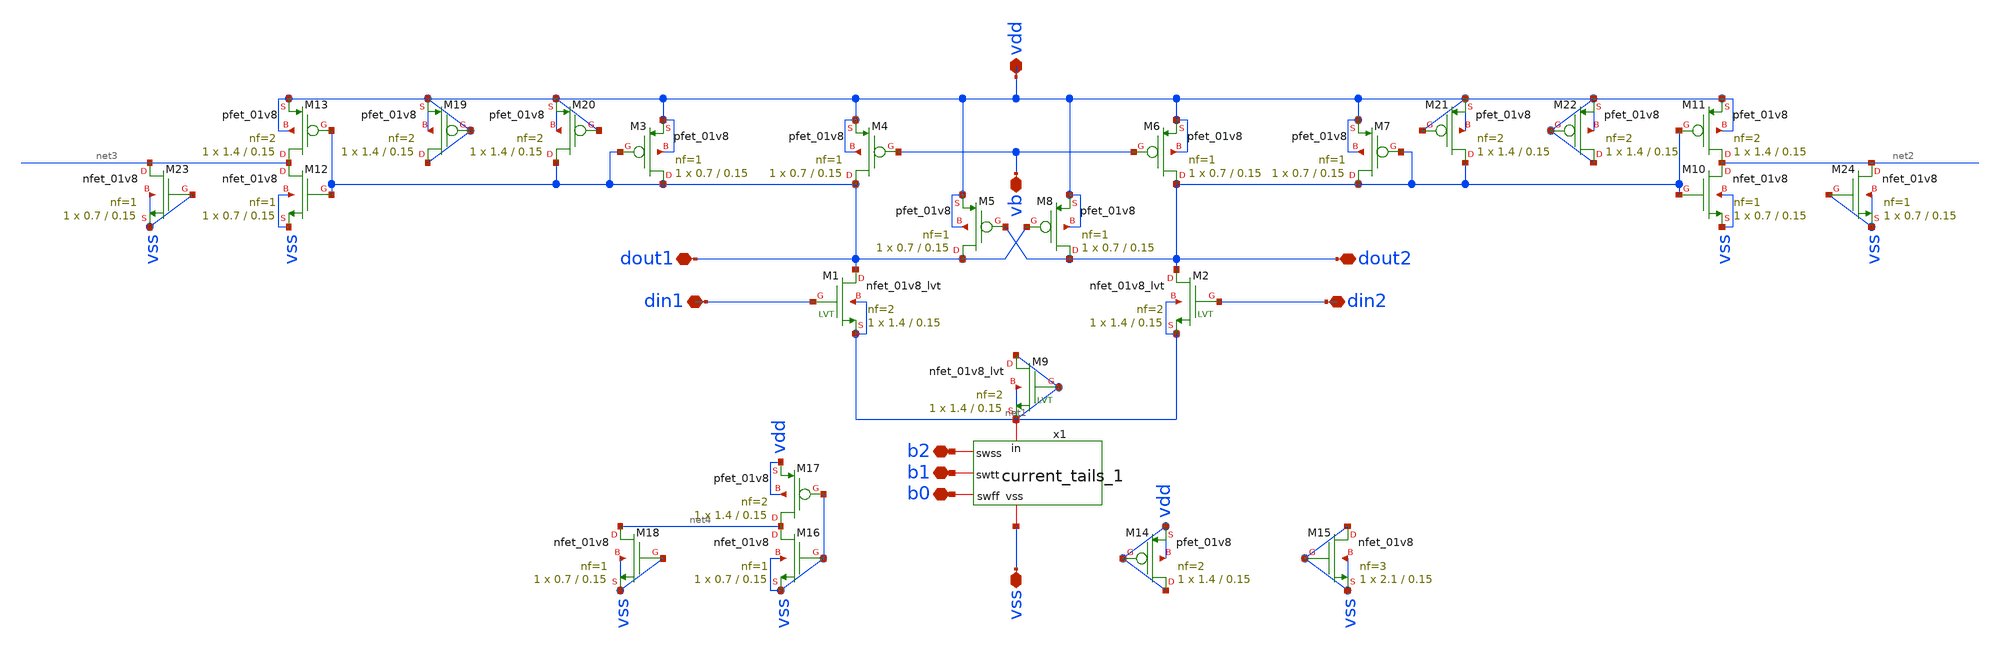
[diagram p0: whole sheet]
** sch_path: xschem/delay_cell_4.sch
**.subckt delay_cell_4 vdd vss vb din1 din2 dout2 dout1 b2 b1 b0
*.iopin vdd
*.iopin vss
*.iopin vb
*.iopin din1
*.iopin din2
*.iopin dout2
*.iopin dout1
*.iopin b2
*.iopin b1
*.iopin b0
XM5 dout1 dout2 vdd vdd sky130_fd_pr__pfet_01v8 L=0.15 W=0.7 nf=1 ad='int((nf+1)/2) * W/nf * 0.29' as='int((nf+2)/2) * W/nf * 0.29'
+ pd='2*int((nf+1)/2) * (W/nf + 0.29)' ps='2*int((nf+2)/2) * (W/nf + 0.29)' nrd='0.29 / W' nrs='0.29 / W'
+ sa=0 sb=0 sd=0 mult=1 m=1
XM8 dout2 dout1 vdd vdd sky130_fd_pr__pfet_01v8 L=0.15 W=0.7 nf=1 ad='int((nf+1)/2) * W/nf * 0.29' as='int((nf+2)/2) * W/nf * 0.29'
+ pd='2*int((nf+1)/2) * (W/nf + 0.29)' ps='2*int((nf+2)/2) * (W/nf + 0.29)' nrd='0.29 / W' nrs='0.29 / W'
+ sa=0 sb=0 sd=0 mult=1 m=1
XM3 dout1 dout1 vdd vdd sky130_fd_pr__pfet_01v8 L=0.15 W=0.7 nf=1 ad='int((nf+1)/2) * W/nf * 0.29' as='int((nf+2)/2) * W/nf * 0.29'
+ pd='2*int((nf+1)/2) * (W/nf + 0.29)' ps='2*int((nf+2)/2) * (W/nf + 0.29)' nrd='0.29 / W' nrs='0.29 / W'
+ sa=0 sb=0 sd=0 mult=1 m=1
XM4 dout1 vb vdd vdd sky130_fd_pr__pfet_01v8 L=0.15 W=0.7 nf=1 ad='int((nf+1)/2) * W/nf * 0.29' as='int((nf+2)/2) * W/nf * 0.29'
+ pd='2*int((nf+1)/2) * (W/nf + 0.29)' ps='2*int((nf+2)/2) * (W/nf + 0.29)' nrd='0.29 / W' nrs='0.29 / W'
+ sa=0 sb=0 sd=0 mult=1 m=1
XM6 dout2 vb vdd vdd sky130_fd_pr__pfet_01v8 L=0.15 W=0.7 nf=1 ad='int((nf+1)/2) * W/nf * 0.29' as='int((nf+2)/2) * W/nf * 0.29'
+ pd='2*int((nf+1)/2) * (W/nf + 0.29)' ps='2*int((nf+2)/2) * (W/nf + 0.29)' nrd='0.29 / W' nrs='0.29 / W'
+ sa=0 sb=0 sd=0 mult=1 m=1
XM7 dout2 dout2 vdd vdd sky130_fd_pr__pfet_01v8 L=0.15 W=0.7 nf=1 ad='int((nf+1)/2) * W/nf * 0.29' as='int((nf+2)/2) * W/nf * 0.29'
+ pd='2*int((nf+1)/2) * (W/nf + 0.29)' ps='2*int((nf+2)/2) * (W/nf + 0.29)' nrd='0.29 / W' nrs='0.29 / W'
+ sa=0 sb=0 sd=0 mult=1 m=1
XM1 dout1 din1 net1 net1 sky130_fd_pr__nfet_01v8_lvt L=0.15 W=1.4 nf=2 ad='int((nf+1)/2) * W/nf * 0.29'
+ as='int((nf+2)/2) * W/nf * 0.29' pd='2*int((nf+1)/2) * (W/nf + 0.29)' ps='2*int((nf+2)/2) * (W/nf + 0.29)'
+ nrd='0.29 / W' nrs='0.29 / W' sa=0 sb=0 sd=0 mult=1 m=1
XM2 dout2 din2 net1 net1 sky130_fd_pr__nfet_01v8_lvt L=0.15 W=1.4 nf=2 ad='int((nf+1)/2) * W/nf * 0.29'
+ as='int((nf+2)/2) * W/nf * 0.29' pd='2*int((nf+1)/2) * (W/nf + 0.29)' ps='2*int((nf+2)/2) * (W/nf + 0.29)'
+ nrd='0.29 / W' nrs='0.29 / W' sa=0 sb=0 sd=0 mult=1 m=1
XM9 net1 net1 net1 net1 sky130_fd_pr__nfet_01v8_lvt L=0.15 W=1.4 nf=2 ad='int((nf+1)/2) * W/nf * 0.29'
+ as='int((nf+2)/2) * W/nf * 0.29' pd='2*int((nf+1)/2) * (W/nf + 0.29)' ps='2*int((nf+2)/2) * (W/nf + 0.29)'
+ nrd='0.29 / W' nrs='0.29 / W' sa=0 sb=0 sd=0 mult=1 m=1
x1 net1 b2 vss b1 b0 current_tails_1
XM10 net2 dout2 vss vss sky130_fd_pr__nfet_01v8 L=0.15 W=0.7 nf=1 ad='int((nf+1)/2) * W/nf * 0.29' as='int((nf+2)/2) * W/nf * 0.29'
+ pd='2*int((nf+1)/2) * (W/nf + 0.29)' ps='2*int((nf+2)/2) * (W/nf + 0.29)' nrd='0.29 / W' nrs='0.29 / W'
+ sa=0 sb=0 sd=0 mult=1 m=1
XM11 net2 dout2 vdd vdd sky130_fd_pr__pfet_01v8 L=0.15 W=1.4 nf=2 ad='int((nf+1)/2) * W/nf * 0.29' as='int((nf+2)/2) * W/nf * 0.29'
+ pd='2*int((nf+1)/2) * (W/nf + 0.29)' ps='2*int((nf+2)/2) * (W/nf + 0.29)' nrd='0.29 / W' nrs='0.29 / W'
+ sa=0 sb=0 sd=0 mult=1 m=1
XM12 net3 dout1 vss vss sky130_fd_pr__nfet_01v8 L=0.15 W=0.7 nf=1 ad='int((nf+1)/2) * W/nf * 0.29' as='int((nf+2)/2) * W/nf * 0.29'
+ pd='2*int((nf+1)/2) * (W/nf + 0.29)' ps='2*int((nf+2)/2) * (W/nf + 0.29)' nrd='0.29 / W' nrs='0.29 / W'
+ sa=0 sb=0 sd=0 mult=1 m=1
XM13 net3 dout1 vdd vdd sky130_fd_pr__pfet_01v8 L=0.15 W=1.4 nf=2 ad='int((nf+1)/2) * W/nf * 0.29' as='int((nf+2)/2) * W/nf * 0.29'
+ pd='2*int((nf+1)/2) * (W/nf + 0.29)' ps='2*int((nf+2)/2) * (W/nf + 0.29)' nrd='0.29 / W' nrs='0.29 / W'
+ sa=0 sb=0 sd=0 mult=1 m=1
XM14 vdd vdd vdd vdd sky130_fd_pr__pfet_01v8 L=0.15 W=1.4 nf=2 ad='int((nf+1)/2) * W/nf * 0.29' as='int((nf+2)/2) * W/nf * 0.29'
+ pd='2*int((nf+1)/2) * (W/nf + 0.29)' ps='2*int((nf+2)/2) * (W/nf + 0.29)' nrd='0.29 / W' nrs='0.29 / W'
+ sa=0 sb=0 sd=0 mult=1 m=1
XM15 vss vss vss vss sky130_fd_pr__nfet_01v8 L=0.15 W=2.1 nf=3 ad='int((nf+1)/2) * W/nf * 0.29' as='int((nf+2)/2) * W/nf * 0.29'
+ pd='2*int((nf+1)/2) * (W/nf + 0.29)' ps='2*int((nf+2)/2) * (W/nf + 0.29)' nrd='0.29 / W' nrs='0.29 / W'
+ sa=0 sb=0 sd=0 mult=1 m=1
XM16 net4 vss vss vss sky130_fd_pr__nfet_01v8 L=0.15 W=0.7 nf=1 ad='int((nf+1)/2) * W/nf * 0.29' as='int((nf+2)/2) * W/nf * 0.29'
+ pd='2*int((nf+1)/2) * (W/nf + 0.29)' ps='2*int((nf+2)/2) * (W/nf + 0.29)' nrd='0.29 / W' nrs='0.29 / W'
+ sa=0 sb=0 sd=0 mult=1 m=1
XM17 net4 vss vdd vdd sky130_fd_pr__pfet_01v8 L=0.15 W=1.4 nf=2 ad='int((nf+1)/2) * W/nf * 0.29' as='int((nf+2)/2) * W/nf * 0.29'
+ pd='2*int((nf+1)/2) * (W/nf + 0.29)' ps='2*int((nf+2)/2) * (W/nf + 0.29)' nrd='0.29 / W' nrs='0.29 / W'
+ sa=0 sb=0 sd=0 mult=1 m=1
XM21 dout2 vdd vdd vdd sky130_fd_pr__pfet_01v8 L=0.15 W=1.4 nf=2 ad='int((nf+1)/2) * W/nf * 0.29' as='int((nf+2)/2) * W/nf * 0.29'
+ pd='2*int((nf+1)/2) * (W/nf + 0.29)' ps='2*int((nf+2)/2) * (W/nf + 0.29)' nrd='0.29 / W' nrs='0.29 / W'
+ sa=0 sb=0 sd=0 mult=1 m=1
XM20 dout1 vdd vdd vdd sky130_fd_pr__pfet_01v8 L=0.15 W=1.4 nf=2 ad='int((nf+1)/2) * W/nf * 0.29' as='int((nf+2)/2) * W/nf * 0.29'
+ pd='2*int((nf+1)/2) * (W/nf + 0.29)' ps='2*int((nf+2)/2) * (W/nf + 0.29)' nrd='0.29 / W' nrs='0.29 / W'
+ sa=0 sb=0 sd=0 mult=1 m=1
XM22 vdd vdd vdd vdd sky130_fd_pr__pfet_01v8 L=0.15 W=1.4 nf=2 ad='int((nf+1)/2) * W/nf * 0.29' as='int((nf+2)/2) * W/nf * 0.29'
+ pd='2*int((nf+1)/2) * (W/nf + 0.29)' ps='2*int((nf+2)/2) * (W/nf + 0.29)' nrd='0.29 / W' nrs='0.29 / W'
+ sa=0 sb=0 sd=0 mult=1 m=1
XM18 net4 vss vss vss sky130_fd_pr__nfet_01v8 L=0.15 W=0.7 nf=1 ad='int((nf+1)/2) * W/nf * 0.29' as='int((nf+2)/2) * W/nf * 0.29'
+ pd='2*int((nf+1)/2) * (W/nf + 0.29)' ps='2*int((nf+2)/2) * (W/nf + 0.29)' nrd='0.29 / W' nrs='0.29 / W'
+ sa=0 sb=0 sd=0 mult=1 m=1
XM19 vdd vdd vdd vdd sky130_fd_pr__pfet_01v8 L=0.15 W=1.4 nf=2 ad='int((nf+1)/2) * W/nf * 0.29' as='int((nf+2)/2) * W/nf * 0.29'
+ pd='2*int((nf+1)/2) * (W/nf + 0.29)' ps='2*int((nf+2)/2) * (W/nf + 0.29)' nrd='0.29 / W' nrs='0.29 / W'
+ sa=0 sb=0 sd=0 mult=1 m=1
XM23 net3 vss vss vss sky130_fd_pr__nfet_01v8 L=0.15 W=0.7 nf=1 ad='int((nf+1)/2) * W/nf * 0.29' as='int((nf+2)/2) * W/nf * 0.29'
+ pd='2*int((nf+1)/2) * (W/nf + 0.29)' ps='2*int((nf+2)/2) * (W/nf + 0.29)' nrd='0.29 / W' nrs='0.29 / W'
+ sa=0 sb=0 sd=0 mult=1 m=1
XM24 net2 vss vss vss sky130_fd_pr__nfet_01v8 L=0.15 W=0.7 nf=1 ad='int((nf+1)/2) * W/nf * 0.29' as='int((nf+2)/2) * W/nf * 0.29'
+ pd='2*int((nf+1)/2) * (W/nf + 0.29)' ps='2*int((nf+2)/2) * (W/nf + 0.29)' nrd='0.29 / W' nrs='0.29 / W'
+ sa=0 sb=0 sd=0 mult=1 m=1
**.ends

* expanding   symbol:  current_tails_1.sym # of pins=5
** sym_path: xschem/current_tails_1.sym
** sch_path: xschem/current_tails_1.sch
.subckt current_tails_1 in swss vss swtt swff
*.iopin in
*.iopin vss
*.iopin swtt
*.iopin swff
*.iopin swss
XM4 in swff vss vss sky130_fd_pr__nfet_01v8 L=0.15 W=0.7 nf=1 ad='int((nf+1)/2) * W/nf * 0.29' as='int((nf+2)/2) * W/nf * 0.29'
+ pd='2*int((nf+1)/2) * (W/nf + 0.29)' ps='2*int((nf+2)/2) * (W/nf + 0.29)' nrd='0.29 / W' nrs='0.29 / W'
+ sa=0 sb=0 sd=0 mult=1 m=1
XM1 in swtt vss vss sky130_fd_pr__nfet_01v8 L=0.15 W=2.1 nf=3 ad='int((nf+1)/2) * W/nf * 0.29' as='int((nf+2)/2) * W/nf * 0.29'
+ pd='2*int((nf+1)/2) * (W/nf + 0.29)' ps='2*int((nf+2)/2) * (W/nf + 0.29)' nrd='0.29 / W' nrs='0.29 / W'
+ sa=0 sb=0 sd=0 mult=1 m=1
XM3 in swss vss vss sky130_fd_pr__nfet_01v8 L=0.15 W=4.2 nf=6 ad='int((nf+1)/2) * W/nf * 0.29' as='int((nf+2)/2) * W/nf * 0.29'
+ pd='2*int((nf+1)/2) * (W/nf + 0.29)' ps='2*int((nf+2)/2) * (W/nf + 0.29)' nrd='0.29 / W' nrs='0.29 / W'
+ sa=0 sb=0 sd=0 mult=1 m=1
XM2 vss vss vss vss sky130_fd_pr__nfet_01v8 L=0.15 W=1.4 nf=2 ad='int((nf+1)/2) * W/nf * 0.29' as='int((nf+2)/2) * W/nf * 0.29'
+ pd='2*int((nf+1)/2) * (W/nf + 0.29)' ps='2*int((nf+2)/2) * (W/nf + 0.29)' nrd='0.29 / W' nrs='0.29 / W'
+ sa=0 sb=0 sd=0 mult=1 m=1
.ends

.end
